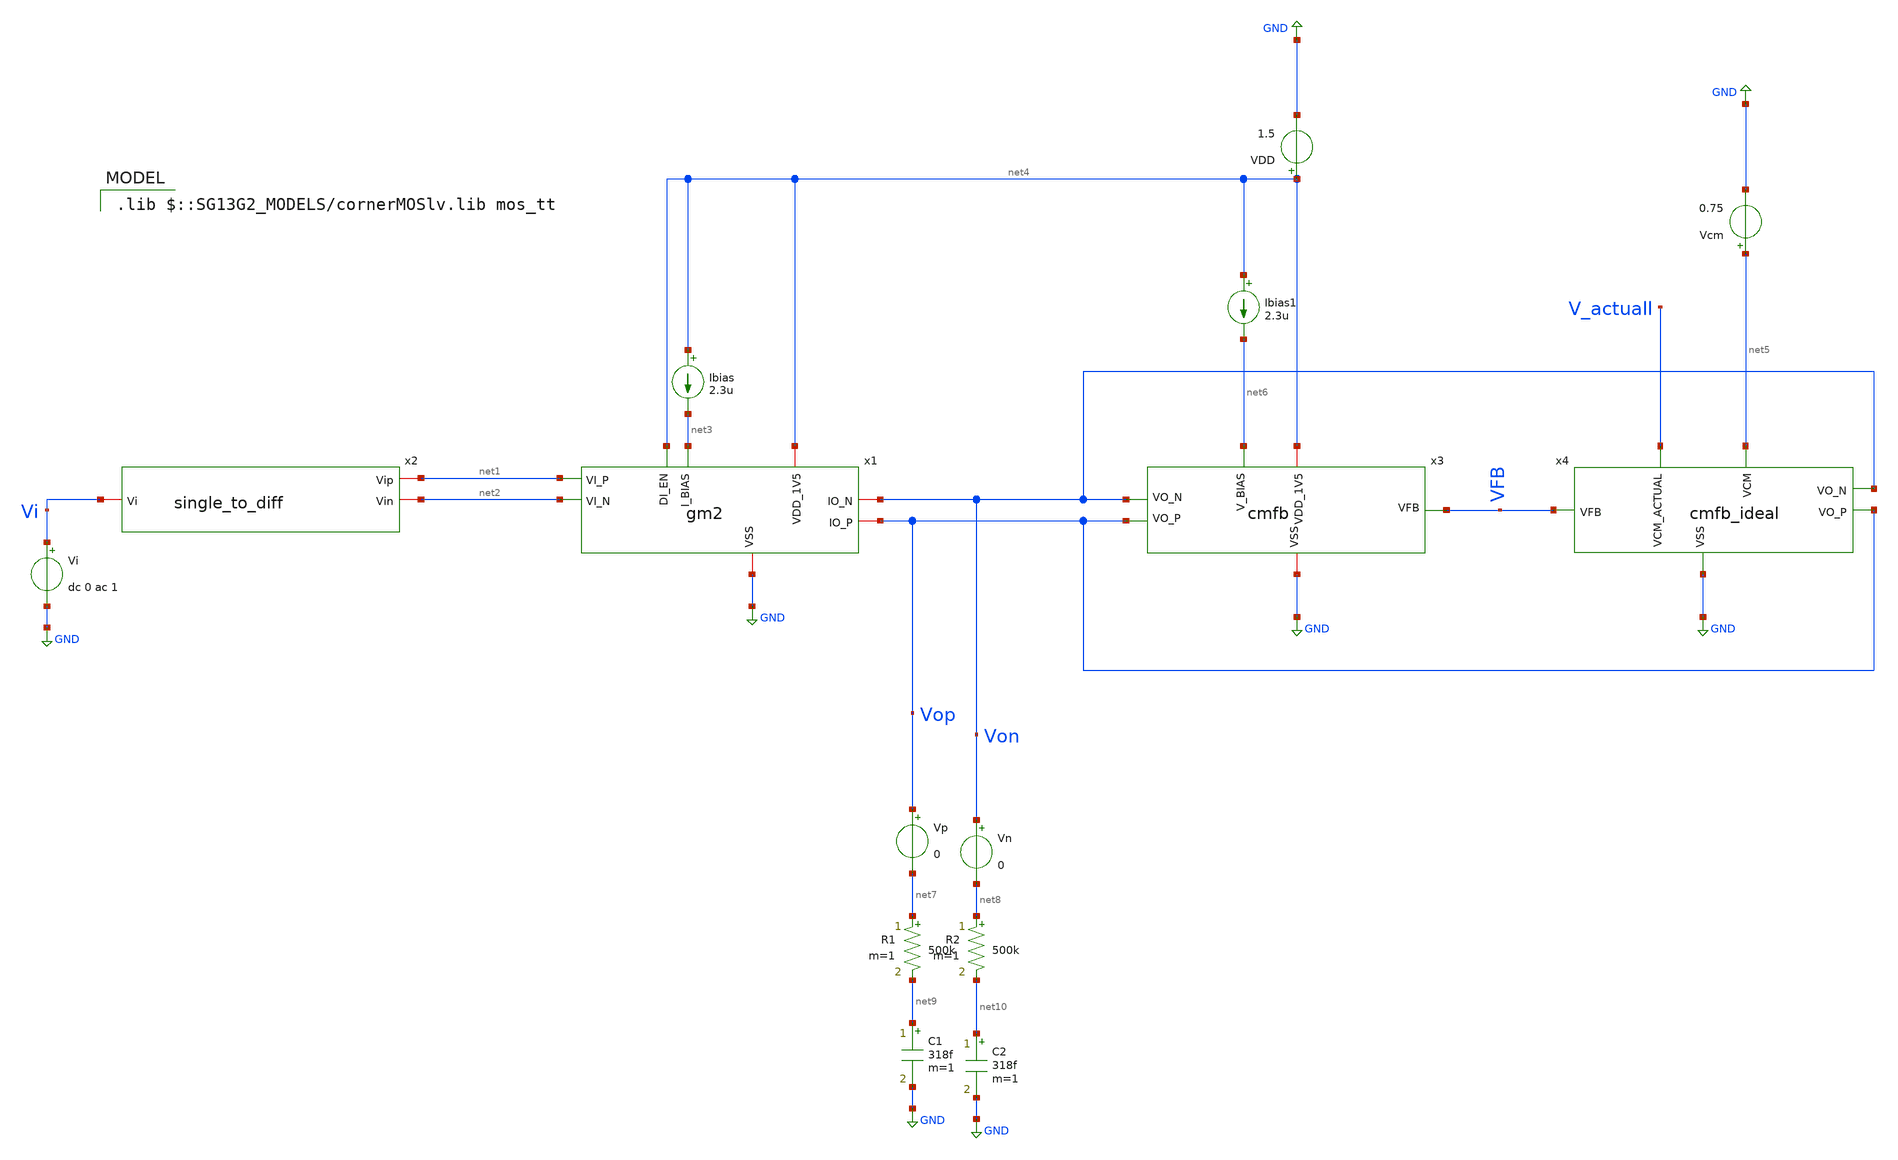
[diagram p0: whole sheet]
** sch_path: gm2_tb_ac.sch
**.subckt gm2_tb_ac
Vi Vi GND dc 0 ac 1
VDD net4 GND 1.5
x1 net4 net3 Von Vop net2 net1 net4 GND gm2
x2 net1 net2 Vi single_to_diff
Ibias net4 net3 2.3u
x3 net4 Vop Von net6 VFB GND cmfb
Vcm net5 GND 0.75
x4 Vop V_actuall Von VFB net5 GND cmfb_ideal
Vp Vop net7 0
Vn Von net8 0
R1 net7 net9 500k m=1
R2 net8 net10 500k m=1
Ibias1 net4 net6 2.3u
C1 net9 GND 318f m=1
C2 net10 GND 318f m=1
**** begin user architecture code
 .lib $::SG13G2_MODELS/cornerMOSlv.lib mos_tt



.temp 27
.control
save all
ac dec 100 1 10G
plot v(vop) v(von)
let gain = db((v(vop)-v(von))/v(vi))
plot gain
meas ac UGBW find frequency when gain=0
print UGBW

noise V(Vop,Von) Vi dec 100 1 5Meg
plot noise1.inoise_spectrum
print inoise_total
op
write gm2_tb_ac.raw
.endc




.save @n.x1.xm1.nsg13_lv_nmos[gm]
.save @n.x1.xm1.nsg13_lv_nmos[vth]
.save @n.x1.xm1.nsg13_lv_nmos[cgg]
.save @n.x1.xm1.nsg13_lv_nmos[vdss]
.save @n.x1.xm1.nsg13_lv_nmos[ids]
.save @n.x1.xm1.nsg13_lv_nmos[vds]
.save @n.x1.xm1.nsg13_lv_nmos[fug]
.save @n.x1.xm1.nsg13_lv_nmos[vgs]


.save @n.x1.xm2.nsg13_lv_nmos[gm]
.save @n.x1.xm2.nsg13_lv_nmos[vth]
.save @n.x1.xm2.nsg13_lv_nmos[cgg]
.save @n.x1.xm2.nsg13_lv_nmos[vdss]
.save @n.x1.xm2.nsg13_lv_nmos[ids]
.save @n.x1.xm2.nsg13_lv_nmos[vds]
.save @n.x1.xm2.nsg13_lv_nmos[fug]
.save @n.x1.xm2.nsg13_lv_nmos[vgs]


.save @n.x1.xm3.nsg13_lv_pmos[gm]
.save @n.x1.xm3.nsg13_lv_pmos[vth]
.save @n.x1.xm3.nsg13_lv_pmos[cgg]
.save @n.x1.xm3.nsg13_lv_pmos[vdss]
.save @n.x1.xm3.nsg13_lv_pmos[ids]
.save @n.x1.xm3.nsg13_lv_pmos[vds]
.save @n.x1.xm3.nsg13_lv_pmos[fug]
.save @n.x1.xm3.nsg13_lv_pmos[vgs]


.save @n.x1.xm4.nsg13_lv_pmos[gm]
.save @n.x1.xm4.nsg13_lv_pmos[vth]
.save @n.x1.xm4.nsg13_lv_pmos[cgg]
.save @n.x1.xm4.nsg13_lv_pmos[vdss]
.save @n.x1.xm4.nsg13_lv_pmos[ids]
.save @n.x1.xm4.nsg13_lv_pmos[vds]
.save @n.x1.xm4.nsg13_lv_pmos[fug]
.save @n.x1.xm4.nsg13_lv_pmos[vgs]


.save @n.x1.xm5.nsg13_lv_nmos[gm]
.save @n.x1.xm5.nsg13_lv_nmos[vth]
.save @n.x1.xm5.nsg13_lv_nmos[cgg]
.save @n.x1.xm5.nsg13_lv_nmos[vdss]
.save @n.x1.xm5.nsg13_lv_nmos[ids]
.save @n.x1.xm5.nsg13_lv_nmos[vds]
.save @n.x1.xm5.nsg13_lv_nmos[fug]
.save @n.x1.xm5.nsg13_lv_nmos[vgs]


.save @n.x1.xm6.nsg13_lv_nmos[gm]
.save @n.x1.xm6.nsg13_lv_nmos[vth]
.save @n.x1.xm6.nsg13_lv_nmos[cgg]
.save @n.x1.xm6.nsg13_lv_nmos[vdss]
.save @n.x1.xm6.nsg13_lv_nmos[ids]
.save @n.x1.xm6.nsg13_lv_nmos[vds]
.save @n.x1.xm6.nsg13_lv_nmos[fug]
.save @n.x1.xm6.nsg13_lv_nmos[vgs]


.save @n.x1.xm7.nsg13_lv_nmos[gm]
.save @n.x1.xm7.nsg13_lv_nmos[vth]
.save @n.x1.xm7.nsg13_lv_nmos[cgg]
.save @n.x1.xm7.nsg13_lv_nmos[vdss]
.save @n.x1.xm7.nsg13_lv_nmos[ids]
.save @n.x1.xm7.nsg13_lv_nmos[vds]
.save @n.x1.xm7.nsg13_lv_nmos[fug]
.save @n.x1.xm7.nsg13_lv_nmos[vgs]


.save @n.x1.xm8.nsg13_lv_pmos[gm]
.save @n.x1.xm8.nsg13_lv_pmos[vth]
.save @n.x1.xm8.nsg13_lv_pmos[cgg]
.save @n.x1.xm8.nsg13_lv_pmos[vdss]
.save @n.x1.xm8.nsg13_lv_pmos[ids]
.save @n.x1.xm8.nsg13_lv_pmos[vds]
.save @n.x1.xm8.nsg13_lv_pmos[fug]
.save @n.x1.xm8.nsg13_lv_pmos[vgs]


.save @n.x1.xm9.nsg13_lv_nmos[gm]
.save @n.x1.xm9.nsg13_lv_nmos[vth]
.save @n.x1.xm9.nsg13_lv_nmos[cgg]
.save @n.x1.xm9.nsg13_lv_nmos[vdss]
.save @n.x1.xm9.nsg13_lv_nmos[ids]
.save @n.x1.xm9.nsg13_lv_nmos[vds]
.save @n.x1.xm9.nsg13_lv_nmos[fug]
.save @n.x1.xm9.nsg13_lv_nmos[vgs]


.save @n.x1.xm10.nsg13_lv_pmos[gm]
.save @n.x1.xm10.nsg13_lv_pmos[vth]
.save @n.x1.xm10.nsg13_lv_pmos[cgg]
.save @n.x1.xm10.nsg13_lv_pmos[vdss]
.save @n.x1.xm10.nsg13_lv_pmos[ids]
.save @n.x1.xm10.nsg13_lv_pmos[vds]
.save @n.x1.xm10.nsg13_lv_pmos[fug]
.save @n.x1.xm10.nsg13_lv_pmos[vgs]


.save @n.x1.xm11.nsg13_lv_nmos[gm]
.save @n.x1.xm11.nsg13_lv_nmos[vth]
.save @n.x1.xm11.nsg13_lv_nmos[cgg]
.save @n.x1.xm11.nsg13_lv_nmos[vdss]
.save @n.x1.xm11.nsg13_lv_nmos[ids]
.save @n.x1.xm11.nsg13_lv_nmos[vds]
.save @n.x1.xm11.nsg13_lv_nmos[fug]
.save @n.x1.xm11.nsg13_lv_nmos[vgs]


.save @n.x1.xm12.nsg13_lv_nmos[gm]
.save @n.x1.xm12.nsg13_lv_nmos[vth]
.save @n.x1.xm12.nsg13_lv_nmos[cgg]
.save @n.x1.xm12.nsg13_lv_nmos[vdss]
.save @n.x1.xm12.nsg13_lv_nmos[ids]
.save @n.x1.xm12.nsg13_lv_nmos[vds]
.save @n.x1.xm12.nsg13_lv_nmos[fug]
.save @n.x1.xm12.nsg13_lv_nmos[vgs]


.save @n.x1.xm13.nsg13_lv_nmos[gm]
.save @n.x1.xm13.nsg13_lv_nmos[vth]
.save @n.x1.xm13.nsg13_lv_nmos[cgg]
.save @n.x1.xm13.nsg13_lv_nmos[vdss]
.save @n.x1.xm13.nsg13_lv_nmos[ids]
.save @n.x1.xm13.nsg13_lv_nmos[vds]
.save @n.x1.xm13.nsg13_lv_nmos[fug]
.save @n.x1.xm13.nsg13_lv_nmos[vgs]


.save @n.x1.xm14.nsg13_lv_pmos[gm]
.save @n.x1.xm14.nsg13_lv_pmos[vth]
.save @n.x1.xm14.nsg13_lv_pmos[cgg]
.save @n.x1.xm14.nsg13_lv_pmos[vdss]
.save @n.x1.xm14.nsg13_lv_pmos[ids]
.save @n.x1.xm14.nsg13_lv_pmos[vds]
.save @n.x1.xm14.nsg13_lv_pmos[fug]
.save @n.x1.xm14.nsg13_lv_pmos[vgs]


.save @n.x1.xm15.nsg13_lv_pmos[gm]
.save @n.x1.xm15.nsg13_lv_pmos[vth]
.save @n.x1.xm15.nsg13_lv_pmos[cgg]
.save @n.x1.xm15.nsg13_lv_pmos[vdss]
.save @n.x1.xm15.nsg13_lv_pmos[ids]
.save @n.x1.xm15.nsg13_lv_pmos[vds]
.save @n.x1.xm15.nsg13_lv_pmos[fug]
.save @n.x1.xm15.nsg13_lv_pmos[vgs]


.save @n.x1.xm16.nsg13_lv_pmos[gm]
.save @n.x1.xm16.nsg13_lv_pmos[vth]
.save @n.x1.xm16.nsg13_lv_pmos[cgg]
.save @n.x1.xm16.nsg13_lv_pmos[vdss]
.save @n.x1.xm16.nsg13_lv_pmos[ids]
.save @n.x1.xm16.nsg13_lv_pmos[vds]
.save @n.x1.xm16.nsg13_lv_pmos[fug]
.save @n.x1.xm16.nsg13_lv_pmos[vgs]


.save @n.x1.xm17.nsg13_lv_pmos[gm]
.save @n.x1.xm17.nsg13_lv_pmos[vth]
.save @n.x1.xm17.nsg13_lv_pmos[cgg]
.save @n.x1.xm17.nsg13_lv_pmos[vdss]
.save @n.x1.xm17.nsg13_lv_pmos[ids]
.save @n.x1.xm17.nsg13_lv_pmos[vds]
.save @n.x1.xm17.nsg13_lv_pmos[fug]
.save @n.x1.xm17.nsg13_lv_pmos[vgs]


.save @n.x1.xm18.nsg13_lv_nmos[gm]
.save @n.x1.xm18.nsg13_lv_nmos[vth]
.save @n.x1.xm18.nsg13_lv_nmos[cgg]
.save @n.x1.xm18.nsg13_lv_nmos[vdss]
.save @n.x1.xm18.nsg13_lv_nmos[ids]
.save @n.x1.xm18.nsg13_lv_nmos[vds]
.save @n.x1.xm18.nsg13_lv_nmos[fug]
.save @n.x1.xm18.nsg13_lv_nmos[vgs]


.save @n.x1.xm19.nsg13_lv_nmos[gm]
.save @n.x1.xm19.nsg13_lv_nmos[vth]
.save @n.x1.xm19.nsg13_lv_nmos[cgg]
.save @n.x1.xm19.nsg13_lv_nmos[vdss]
.save @n.x1.xm19.nsg13_lv_nmos[ids]
.save @n.x1.xm19.nsg13_lv_nmos[vds]
.save @n.x1.xm19.nsg13_lv_nmos[fug]
.save @n.x1.xm19.nsg13_lv_nmos[vgs]


.save @n.x1.xm20.nsg13_lv_nmos[gm]
.save @n.x1.xm20.nsg13_lv_nmos[vth]
.save @n.x1.xm20.nsg13_lv_nmos[cgg]
.save @n.x1.xm20.nsg13_lv_nmos[vdss]
.save @n.x1.xm20.nsg13_lv_nmos[ids]
.save @n.x1.xm20.nsg13_lv_nmos[vds]
.save @n.x1.xm20.nsg13_lv_nmos[fug]
.save @n.x1.xm20.nsg13_lv_nmos[vgs]


.save @n.x1.xm21.nsg13_lv_nmos[gm]
.save @n.x1.xm21.nsg13_lv_nmos[vth]
.save @n.x1.xm21.nsg13_lv_nmos[cgg]
.save @n.x1.xm21.nsg13_lv_nmos[vdss]
.save @n.x1.xm21.nsg13_lv_nmos[ids]
.save @n.x1.xm21.nsg13_lv_nmos[vds]
.save @n.x1.xm21.nsg13_lv_nmos[fug]
.save @n.x1.xm21.nsg13_lv_nmos[vgs]

.save @n.x3.xm2.nsg13_lv_nmos[gm]
.save @n.x3.xm2.nsg13_lv_nmos[vth]
.save @n.x3.xm2.nsg13_lv_nmos[cgg]
.save @n.x3.xm2.nsg13_lv_nmos[vdss]
.save @n.x3.xm2.nsg13_lv_nmos[ids]
.save @n.x3.xm2.nsg13_lv_nmos[vds]
.save @n.x3.xm2.nsg13_lv_nmos[fug]
.save @n.x3.xm2.nsg13_lv_nmos[vgs]


.save @n.x3.xm3.nsg13_lv_nmos[gm]
.save @n.x3.xm3.nsg13_lv_nmos[vth]
.save @n.x3.xm3.nsg13_lv_nmos[cgg]
.save @n.x3.xm3.nsg13_lv_nmos[vdss]
.save @n.x3.xm3.nsg13_lv_nmos[ids]
.save @n.x3.xm3.nsg13_lv_nmos[vds]
.save @n.x3.xm3.nsg13_lv_nmos[fug]
.save @n.x3.xm3.nsg13_lv_nmos[vgs]

.save @n.x3.xm1.nsg13_lv_pmos[gm]
.save @n.x3.xm1.nsg13_lv_pmos[vth]
.save @n.x3.xm1.nsg13_lv_pmos[cgg]
.save @n.x3.xm1.nsg13_lv_pmos[vdss]
.save @n.x3.xm1.nsg13_lv_pmos[ids]
.save @n.x3.xm1.nsg13_lv_pmos[vds]
.save @n.x3.xm1.nsg13_lv_pmos[fug]
.save @n.x1.xm1.nsg13_lv_pmos[vgs]

.save @n.x3.xm14.nsg13_lv_pmos[gm]
.save @n.x3.xm14.nsg13_lv_pmos[vth]
.save @n.x3.xm14.nsg13_lv_pmos[cgg]
.save @n.x3.xm14.nsg13_lv_pmos[vdss]
.save @n.x3.xm14.nsg13_lv_pmos[ids]
.save @n.x3.xm14.nsg13_lv_pmos[vds]
.save @n.x3.xm14.nsg13_lv_pmos[fug]
.save @n.x3.xm14.nsg13_lv_pmos[vgs]


.save @n.x3.xm4.nsg13_lv_pmos[gm]
.save @n.x3.xm4.nsg13_lv_pmos[vth]
.save @n.x3.xm4.nsg13_lv_pmos[cgg]
.save @n.x3.xm4.nsg13_lv_pmos[vdss]
.save @n.x3.xm4.nsg13_lv_pmos[ids]
.save @n.x3.xm4.nsg13_lv_pmos[vds]
.save @n.x3.xm4.nsg13_lv_pmos[fug]
.save @n.x3.xm4.nsg13_lv_pmos[vgs]

.save @n.x3.xm5.nsg13_lv_nmos[gm]
.save @n.x3.xm5.nsg13_lv_nmos[vth]
.save @n.x3.xm5.nsg13_lv_nmos[cgg]
.save @n.x3.xm5.nsg13_lv_nmos[vdss]
.save @n.x3.xm5.nsg13_lv_nmos[ids]
.save @n.x3.xm5.nsg13_lv_nmos[vds]
.save @n.x3.xm5.nsg13_lv_nmos[fug]
.save @n.x3.xm5.nsg13_lv_nmos[vgs]












**** end user architecture code
**.ends

* expanding   symbol:  gm2.sym # of pins=8
** sym_path: gm2.sym
** sch_path: gm2.sch
.subckt gm2 VDD_1V5 I_BIAS IO_N IO_P VI_N VI_P DI_EN VSS
*.ipin VI_N
*.ipin VI_P
*.iopin VSS
*.iopin VDD_1V5
*.iopin IO_P
*.iopin IO_N
*.ipin I_BIAS
*.ipin DI_EN
XM1 I_drain1 VI_P Vsp Vsp sg13_lv_nmos w=1u l=1u ng=1 m=1 mm_ok=1
XM2 I_drain2 VI_N Vsn Vsn sg13_lv_nmos w=1u l=1u ng=1 m=1 mm_ok=1
Rs Vsp Vsn 500k m=1
XM5 Vsp V_dg VSS VSS sg13_lv_nmos w=0.5u l=1u ng=1 m=1 mm_ok=1
XM6 Vsn V_dg VSS VSS sg13_lv_nmos w=0.5u l=1u ng=1 m=1 mm_ok=1
XM7 V_dg V_dg VSS VSS sg13_lv_nmos w=1u l=1u ng=1 m=1 mm_ok=1
XM8 net1 DI_EN VDD_1V5 VDD_1V5 sg13_lv_pmos w=1u l=0.13u ng=1 m=1 mm_ok=1
XM9 enable net1 VSS VSS sg13_lv_nmos w=1u l=0.13u ng=1 m=1 mm_ok=1
XM10 enable net1 VDD_1V5 VDD_1V5 sg13_lv_pmos w=1u l=0.13u ng=1 m=1 mm_ok=1
XM11 net1 DI_EN VSS VSS sg13_lv_nmos w=1u l=0.13u ng=1 m=1 mm_ok=1
XM12 I_BIAS enable V_dg VSS sg13_lv_nmos w=1u l=0.13u ng=1 m=1 mm_ok=1
XM3 I_drain1 I_drain1 VDD_1V5 VDD_1V5 sg13_lv_pmos w=1u l=1u ng=1 m=1 mm_ok=1
XM4 I_drain2 I_drain2 VDD_1V5 VDD_1V5 sg13_lv_pmos w=1u l=1u ng=1 m=1 mm_ok=1
XM14 Vds_1 I_drain1 VDD_1V5 VDD_1V5 sg13_lv_pmos w=1u l=1u ng=1 m=1 mm_ok=1
XM15 Vds_2 I_drain2 VDD_1V5 VDD_1V5 sg13_lv_pmos w=1u l=1u ng=1 m=1 mm_ok=1
XM13 V_dg net1 VSS VSS sg13_lv_nmos w=1u l=1u ng=1 m=1 mm_ok=1
XM16 IO_P I_drain1 VDD_1V5 VDD_1V5 sg13_lv_pmos w=2u l=1u ng=1 m=1 mm_ok=1
XM17 IO_N I_drain2 VDD_1V5 VDD_1V5 sg13_lv_pmos w=2u l=1u ng=1 m=1 mm_ok=1
XM18 IO_P Vds_1 VSS VSS sg13_lv_nmos w=0.74u l=1u ng=1 m=1 mm_ok=1
XM19 Vds_1 Vds_1 VSS VSS sg13_lv_nmos w=1u l=1u ng=1 m=1 mm_ok=1
XM20 Vds_2 Vds_2 VSS VSS sg13_lv_nmos w=1u l=1u ng=1 m=1 mm_ok=1
XM21 IO_N Vds_2 VSS VSS sg13_lv_nmos w=0.74u l=1u ng=1 m=1 mm_ok=1
.ends


* expanding   symbol:  single_to_diff.sym # of pins=3
** sym_path: single_to_diff.sym
** sch_path: single_to_diff.sch
.subckt single_to_diff Vip Vin Vi
*.iopin Vi
*.iopin Vip
*.iopin Vin
E1 net1 GND Vi GND 1
E2 Vin net2 net1 GND -0.5
E3 Vip net2 net1 GND 0.5
Vcm net2 GND 0.75
.ends


* expanding   symbol:  cmfb.sym # of pins=6
** sym_path: cmfb.sym
** sch_path: cmfb.sch
.subckt cmfb VDD_1V5 VO_P VO_N V_BIAS VFB VSS
*.iopin VDD_1V5
*.iopin VSS
*.ipin V_BIAS
*.ipin VFB
*.opin VO_P
*.opin VO_N
XM14 VO_P VFB VDD_1V5 VDD_1V5 sg13_lv_pmos w=1u l=1u ng=1 m=1 mm_ok=1
XM1 VO_N VFB VDD_1V5 VDD_1V5 sg13_lv_pmos w=1u l=1u ng=1 m=1 mm_ok=1
XM2 VO_P V_BIAS VSS VSS sg13_lv_nmos w=1u l=1u ng=1 m=1 mm_ok=1
XM3 VO_N V_BIAS VSS VSS sg13_lv_nmos w=1u l=1u ng=1 m=1 mm_ok=1
XM5 V_BIAS V_BIAS VSS VSS sg13_lv_nmos w=1u l=1u ng=1 m=1 mm_ok=1
.ends


* expanding   symbol:  cmfb_ideal.sym # of pins=6
** sym_path: cmfb_ideal.sym
** sch_path: cmfb_ideal.sch
.subckt cmfb_ideal VO_P VCM_ACTUAL VO_N VFB VCM VSS
*.ipin VO_P
*.ipin VO_N
*.ipin VCM
*.ipin VSS
*.opin VFB
*.opin VCM_ACTUAL
E3 net1 VSS VO_N VSS -1
E4 total VSS VO_P net1 1
E5 VCM_ACTUAL VSS total VSS 0.5
E6 VFB VSS VCM VCM_ACTUAL -40
.ends

.GLOBAL GND
.end
